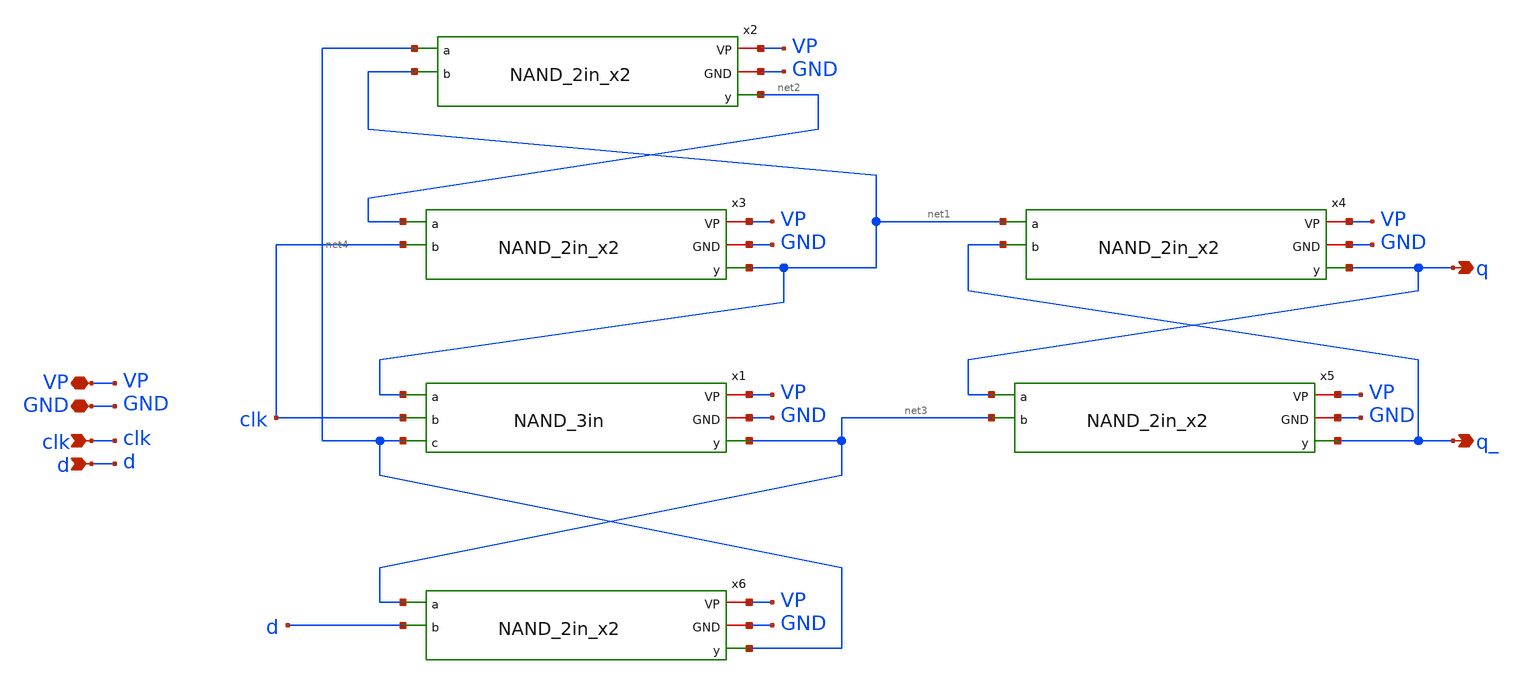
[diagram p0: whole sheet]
** sch_path: schematics/divider/schematics/d_flip_flop.sch
**.subckt d_flip_flop GND clk VP d q q_
*.iopin GND
*.ipin clk
*.iopin VP
*.ipin d
*.opin q
*.opin q_
x1 VP GND net1 net3 clk net4 NAND_3in
x2 VP GND net4 net2 net1 NAND_2in_x2
x3 VP GND net2 net1 clk NAND_2in_x2
x4 VP GND net1 q q_ NAND_2in_x2
x5 VP GND q q_ net3 NAND_2in_x2
x6 VP GND net3 net4 d NAND_2in_x2
**.ends

* expanding   symbol:  /foss/designs/CHIP-PLL/schematics/divider/schematics/NAND_3in.sym # of pins=6
** sym_path: schematics/divider/schematics/NAND_3in.sym
** sch_path: schematics/divider/schematics/NAND_3in.sch
.subckt NAND_3in VP GND a y b c
*.opin y
*.iopin GND
*.ipin a
*.iopin VP
*.ipin b
*.ipin c
XM1 y a net2 GND sg13_lv_nmos w=0.15u l=0.13u ng=1 m=1 mm_ok=1
XM3 net2 b net1 GND sg13_lv_nmos w=0.15u l=0.13u ng=1 m=1 mm_ok=1
XM4 net1 c GND GND sg13_lv_nmos w=0.15u l=0.13u ng=1 m=1 mm_ok=1
XM7 y c VP VP sg13_lv_pmos w=0.15u l=0.13u ng=1 m=1 mm_ok=1
XM2 y a VP VP sg13_lv_pmos w=0.15u l=0.13u ng=1 m=1 mm_ok=1
XM5 y b VP VP sg13_lv_pmos w=0.15u l=0.13u ng=1 m=1 mm_ok=1
.ends


* expanding   symbol:  /foss/designs/CHIP-PLL/schematics/divider/schematics/NAND_2in_x2.sym # of
*+ pins=5
** sym_path: schematics/divider/schematics/NAND_2in_x2.sym
** sch_path: schematics/divider/schematics/NAND_2in_x2.sch
.subckt NAND_2in_x2 VP GND a y b
*.opin y
*.iopin GND
*.ipin a
*.iopin VP
*.ipin b
XM1 y a net1 GND sg13_lv_nmos w=0.6u l=0.13u ng=1 m=1 mm_ok=1
XM2 y b VP VP sg13_lv_pmos w=0.3u l=0.13u ng=1 m=1 mm_ok=1
XM3 net1 b GND GND sg13_lv_nmos w=0.6u l=0.13u ng=1 m=1 mm_ok=1
XM4 y a VP VP sg13_lv_pmos w=0.3u l=0.13u ng=1 m=1 mm_ok=1
.ends

.end
